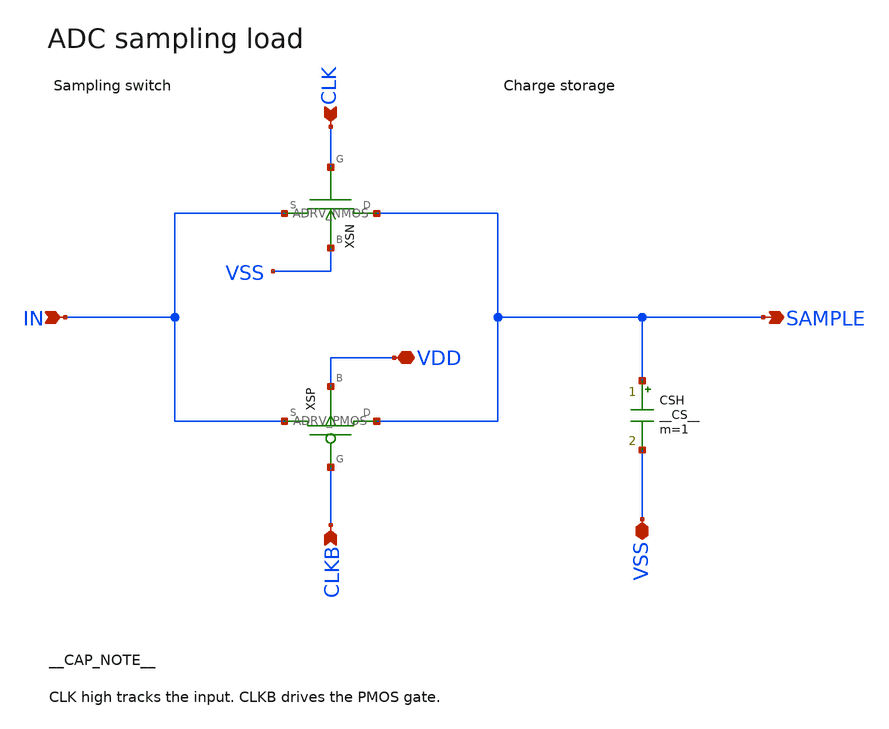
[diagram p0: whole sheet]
** sch_path: examples/sky130-adc-driver/ADRV_SAMPLER.sch
**.subckt ADRV_SAMPLER IN SAMPLE CLK CLKB VDD VSS
*.ipin IN
*.opin SAMPLE
*.ipin CLK
*.ipin CLKB
*.iopin VDD
*.iopin VSS
XSN SAMPLE CLK IN VSS sky130_fd_pr__nfet_01v8 w=1 l=1 nf=1 ad=0.3 as=0.3 pd=2.6 ps=2.6 m=1
XSP SAMPLE CLKB IN VDD sky130_fd_pr__pfet_01v8 w=1 l=1 nf=1 ad=0.3 as=0.3 pd=2.6 ps=2.6 m=1
CSH SAMPLE VSS __CS__ m=1
**.ends
.end
